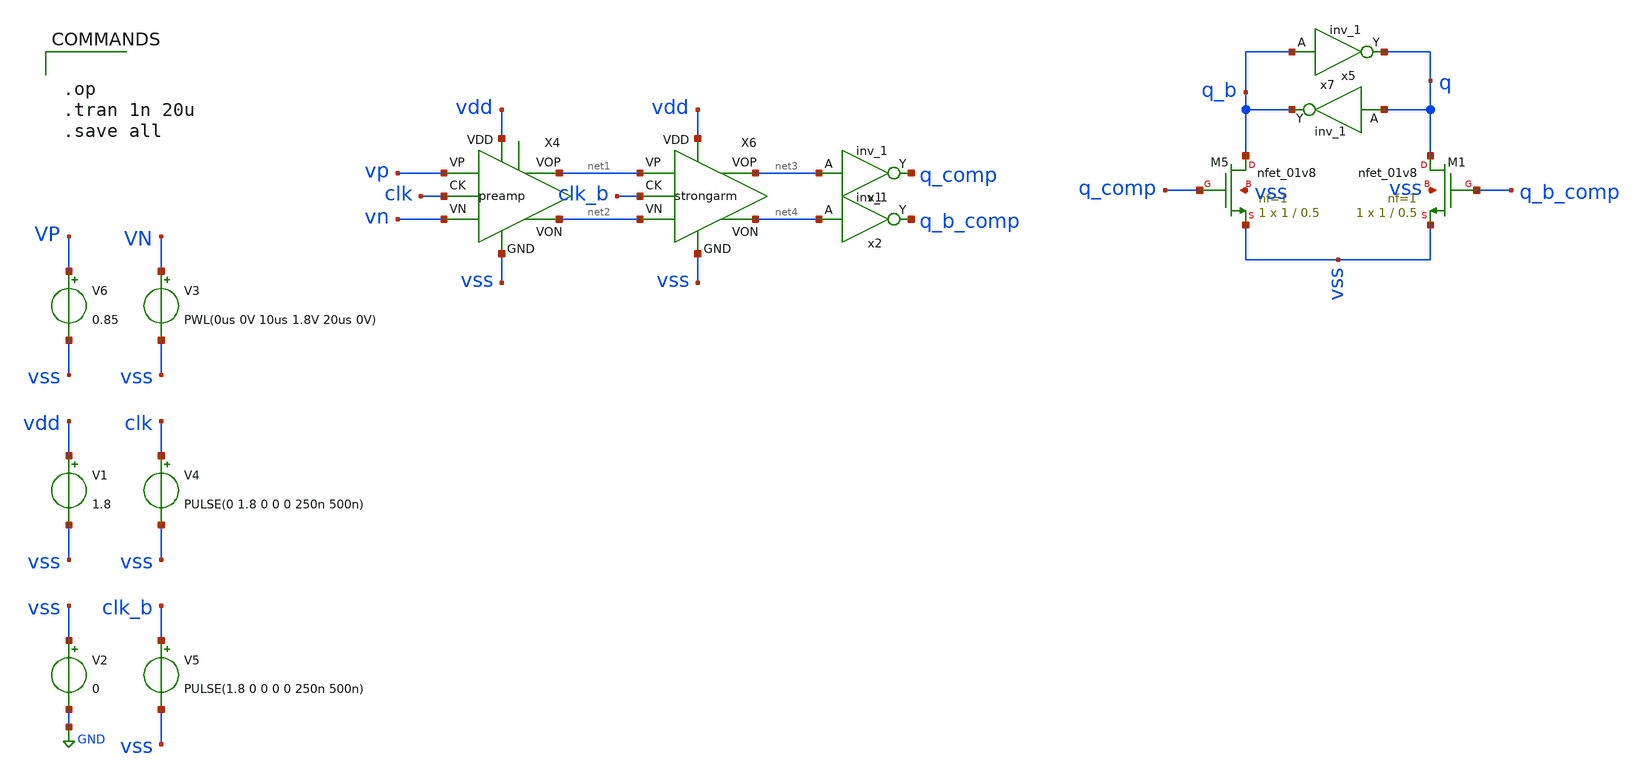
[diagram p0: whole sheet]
** sch_path: xschem/comparator/comparator_tb.sch
.lib $::SKYWATER_MODELS/sky130.lib.spice tt
.include $::SKYWATER_STDCELLS/sky130_fd_sc_hd.spice

**.subckt comparator_tb
V1 vdd vss 1.8
V3 VN vss PWL(0us 0V 10us 1.8V 20us 0V)
V4 clk vss PULSE(0 1.8 0 0 0 250n 500n)
V5 clk_b vss PULSE(1.8 0 0 0 0 250n 500n)
V6 VP vss 0.85
X4 vp vn vss net2 net1 vdd clk preamp
X6 net1 net2 vss net4 net3 vdd clk_b strongarm
XM5 q_b q_comp vss vss sky130_fd_pr__nfet_01v8 L=0.5 W=1 nf=1 ad='int((1 + 1)/2) * 1 / 1 * 0.29' as='int((1 + 2)/2) * 1 / 1 * 0.29'
+ pd='2*int((1 + 1)/2) * (1 / 1 + 0.29)' ps='2*int((1 + 2)/2) * (1 / 1 + 0.29)' nrd='0.29 / 1 ' nrs='0.29 / 1 '
+ sa=0 sb=0 sd=0 mult=1 m=1
XM1 q q_b_comp vss vss sky130_fd_pr__nfet_01v8 L=0.5 W=1 nf=1 ad='int((1 + 1)/2) * 1 / 1 * 0.29' as='int((1 + 2)/2) * 1 / 1 * 0.29'
+ pd='2*int((1 + 1)/2) * (1 / 1 + 0.29)' ps='2*int((1 + 2)/2) * (1 / 1 + 0.29)' nrd='0.29 / 1 ' nrs='0.29 / 1 '
+ sa=0 sb=0 sd=0 mult=1 m=1
x5 q_b vss vss vdd vdd q sky130_fd_sc_hd__inv_1
x7 q vss vss vdd vdd q_b sky130_fd_sc_hd__inv_1
V2 vss GND 0
x1 net3 vss vss vdd vdd q_comp sky130_fd_sc_hd__inv_1
x2 net4 vss vss vdd vdd q_b_comp sky130_fd_sc_hd__inv_1
**** begin user architecture code


.op
.tran 1n 20u
.save all


**** end user architecture code
**.ends

* expanding   symbol:  xschem/comparator/preamp.sym # of pins=7
** sym_path: xschem/comparator/preamp.sym
** sch_path: xschem/comparator/preamp.sch
.subckt preamp VP VN GND VON VOP VDD CK
*.iopin VDD
*.iopin GND
*.iopin CK
*.iopin VON
*.iopin VOP
*.iopin VP
*.iopin VN
XM5 VON VP net1 GND sky130_fd_pr__nfet_01v8 L=1.5 W=2.5 nf=2 ad='int((2 + 1)/2) * 2.5 / 2 * 0.29' as='int((2 + 2)/2) * 2.5 / 2 * 0.29'
+ pd='2*int((2 + 1)/2) * (2.5 / 2 + 0.29)' ps='2*int((2 + 2)/2) * (2.5 / 2 + 0.29)' nrd='0.29 / 2.5 ' nrs='0.29 / 2.5 '
+ sa=0 sb=0 sd=0 mult=1 m=1
XM6 VON CK VDD VDD sky130_fd_pr__pfet_01v8 L=0.5 W=4 nf=1 ad='int((nf+1)/2) * W/nf * 0.29' as='int((nf+2)/2) * W/nf * 0.29'
+ pd='2*int((nf+1)/2) * (W/nf + 0.29)' ps='2*int((nf+2)/2) * (W/nf + 0.29)' nrd='0.29 / W' nrs='0.29 / W'
+ sa=0 sb=0 sd=0 mult=1 m=1
XM7 VOP CK VDD VDD sky130_fd_pr__pfet_01v8 L=0.5 W=4 nf=1 ad='int((nf+1)/2) * W/nf * 0.29' as='int((nf+2)/2) * W/nf * 0.29'
+ pd='2*int((nf+1)/2) * (W/nf + 0.29)' ps='2*int((nf+2)/2) * (W/nf + 0.29)' nrd='0.29 / W' nrs='0.29 / W'
+ sa=0 sb=0 sd=0 mult=1 m=1
XM8 VOP VN net1 GND sky130_fd_pr__nfet_01v8 L=1.5 W=2.5 nf=2 ad='int((2 + 1)/2) * 2.5 / 2 * 0.29' as='int((2 + 2)/2) * 2.5 / 2 * 0.29'
+ pd='2*int((2 + 1)/2) * (2.5 / 2 + 0.29)' ps='2*int((2 + 2)/2) * (2.5 / 2 + 0.29)' nrd='0.29 / 2.5 ' nrs='0.29 / 2.5 '
+ sa=0 sb=0 sd=0 mult=1 m=1
XM9 net1 CK GND GND sky130_fd_pr__nfet_01v8 L=2 W=4 nf=1 ad='int((1 + 1)/2) * 4 / 1 * 0.29' as='int((1 + 2)/2) * 4 / 1 * 0.29'
+ pd='2*int((1 + 1)/2) * (4 / 1 + 0.29)' ps='2*int((1 + 2)/2) * (4 / 1 + 0.29)' nrd='0.29 / 4 ' nrs='0.29 / 4 '
+ sa=0 sb=0 sd=0 mult=1 m=1
.ends


* expanding   symbol:  xschem/comparator/strongarm.sym # of pins=7
** sym_path: xschem/comparator/strongarm.sym
** sch_path: xschem/comparator/strongarm.sch
.subckt strongarm VP VN GND VON VOP VDD CK
*.iopin GND
*.ipin VP
*.opin VOP
*.opin VON
*.ipin VN
*.iopin VDD
*.ipin CK
XM2 net2 CK GND GND sky130_fd_pr__nfet_01v8 L=0.15 W=2 nf=2 ad='int((nf+1)/2) * W/nf * 0.29' as='int((nf+2)/2) * W/nf * 0.29'
+ pd='2*int((nf+1)/2) * (W/nf + 0.29)' ps='2*int((nf+2)/2) * (W/nf + 0.29)' nrd='0.29 / W' nrs='0.29 / W'
+ sa=0 sb=0 sd=0 mult=1 m=1
XM4 VON CK VDD VDD sky130_fd_pr__pfet_01v8 L=0.15 W=1 nf=1 ad='int((nf+1)/2) * W/nf * 0.29' as='int((nf+2)/2) * W/nf * 0.29'
+ pd='2*int((nf+1)/2) * (W/nf + 0.29)' ps='2*int((nf+2)/2) * (W/nf + 0.29)' nrd='0.29 / W' nrs='0.29 / W'
+ sa=0 sb=0 sd=0 mult=1 m=1
XM5 net1 CK VDD VDD sky130_fd_pr__pfet_01v8 L=0.15 W=1 nf=1 ad='int((nf+1)/2) * W/nf * 0.29' as='int((nf+2)/2) * W/nf * 0.29'
+ pd='2*int((nf+1)/2) * (W/nf + 0.29)' ps='2*int((nf+2)/2) * (W/nf + 0.29)' nrd='0.29 / W' nrs='0.29 / W'
+ sa=0 sb=0 sd=0 mult=1 m=1
XM8 net1 VP net2 GND sky130_fd_pr__nfet_01v8 L=0.15 W=10 nf=1 ad='int((nf+1)/2) * W/nf * 0.29' as='int((nf+2)/2) * W/nf * 0.29'
+ pd='2*int((nf+1)/2) * (W/nf + 0.29)' ps='2*int((nf+2)/2) * (W/nf + 0.29)' nrd='0.29 / W' nrs='0.29 / W'
+ sa=0 sb=0 sd=0 mult=1 m=1
XM9 VON VOP net1 GND sky130_fd_pr__nfet_01v8 L=0.15 W=2.5 nf=4 ad='int((nf+1)/2) * W/nf * 0.29' as='int((nf+2)/2) * W/nf * 0.29'
+ pd='2*int((nf+1)/2) * (W/nf + 0.29)' ps='2*int((nf+2)/2) * (W/nf + 0.29)' nrd='0.29 / W' nrs='0.29 / W'
+ sa=0 sb=0 sd=0 mult=1 m=1
XM10 VON VOP VDD VDD sky130_fd_pr__pfet_01v8 L=0.15 W=2.5 nf=1 ad='int((nf+1)/2) * W/nf * 0.29' as='int((nf+2)/2) * W/nf * 0.29'
+ pd='2*int((nf+1)/2) * (W/nf + 0.29)' ps='2*int((nf+2)/2) * (W/nf + 0.29)' nrd='0.29 / W' nrs='0.29 / W'
+ sa=0 sb=0 sd=0 mult=1 m=1
XM11 VOP CK VDD VDD sky130_fd_pr__pfet_01v8 L=0.15 W=1 nf=1 ad='int((nf+1)/2) * W/nf * 0.29' as='int((nf+2)/2) * W/nf * 0.29'
+ pd='2*int((nf+1)/2) * (W/nf + 0.29)' ps='2*int((nf+2)/2) * (W/nf + 0.29)' nrd='0.29 / W' nrs='0.29 / W'
+ sa=0 sb=0 sd=0 mult=1 m=1
XM12 net3 CK VDD VDD sky130_fd_pr__pfet_01v8 L=0.15 W=1 nf=1 ad='int((nf+1)/2) * W/nf * 0.29' as='int((nf+2)/2) * W/nf * 0.29'
+ pd='2*int((nf+1)/2) * (W/nf + 0.29)' ps='2*int((nf+2)/2) * (W/nf + 0.29)' nrd='0.29 / W' nrs='0.29 / W'
+ sa=0 sb=0 sd=0 mult=1 m=1
XM13 net3 VN net2 GND sky130_fd_pr__nfet_01v8 L=0.15 W=10 nf=1 ad='int((nf+1)/2) * W/nf * 0.29' as='int((nf+2)/2) * W/nf * 0.29'
+ pd='2*int((nf+1)/2) * (W/nf + 0.29)' ps='2*int((nf+2)/2) * (W/nf + 0.29)' nrd='0.29 / W' nrs='0.29 / W'
+ sa=0 sb=0 sd=0 mult=1 m=1
XM14 VOP VON net3 GND sky130_fd_pr__nfet_01v8 L=0.15 W=10 nf=1 ad='int((nf+1)/2) * W/nf * 0.29' as='int((nf+2)/2) * W/nf * 0.29'
+ pd='2*int((nf+1)/2) * (W/nf + 0.29)' ps='2*int((nf+2)/2) * (W/nf + 0.29)' nrd='0.29 / W' nrs='0.29 / W'
+ sa=0 sb=0 sd=0 mult=1 m=1
XM15 VOP VON VDD VDD sky130_fd_pr__pfet_01v8 L=0.15 W=2.5 nf=1 ad='int((nf+1)/2) * W/nf * 0.29' as='int((nf+2)/2) * W/nf * 0.29'
+ pd='2*int((nf+1)/2) * (W/nf + 0.29)' ps='2*int((nf+2)/2) * (W/nf + 0.29)' nrd='0.29 / W' nrs='0.29 / W'
+ sa=0 sb=0 sd=0 mult=1 m=1
.ends

.GLOBAL GND
.end
